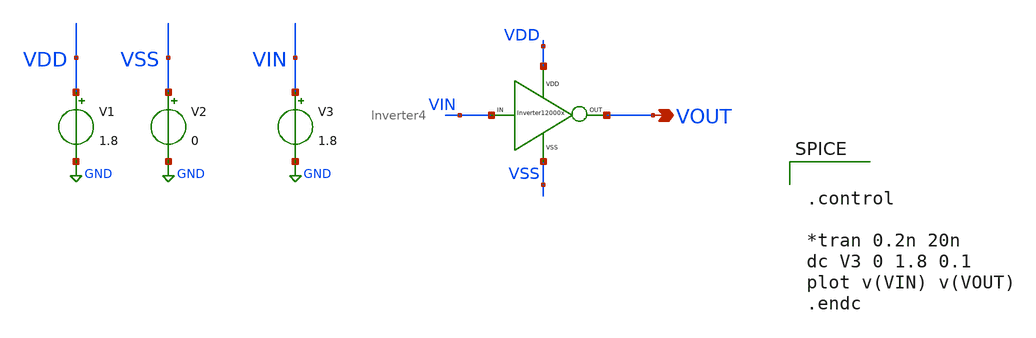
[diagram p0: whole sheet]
** sch_path: xschem/DC_DC_Converter_xschem/OTHERS/DC_DC_Converter0/Inverter_4/Inverter4_TB.sch
**.subckt Inverter4_TB VOUT
*.opin VOUT
V1 VDD GND 1.8
V2 VSS GND 0
V3 VIN GND 1.8
X1 VIN VOUT VDD VSS Inverter4
**** begin user architecture code


.control

*tran 0.2n 20n
dc V3 0 1.8 0.1
plot v(VIN) v(VOUT)
.endc



** opencircuitdesign pdks install
.lib $::SKYWATER_MODELS/sky130.lib.spice tt


**** end user architecture code
**.ends

* expanding   symbol:  DC_DC_Converter/Inverter_4/Inverter4.sym # of pins=4
** sym_path: xschem/DC_DC_Converter_xschem/OTHERS/DC_DC_Converter0/Inverter_4/Inverter4.sym
** sch_path: xschem/DC_DC_Converter_xschem/OTHERS/DC_DC_Converter0/Inverter_4/Inverter4.sch
.subckt Inverter4 VIN VOUT VDD VSS
*.ipin VIN
*.iopin VDD
*.iopin VSS
*.opin VOUT
XM1 net2 VIN VSS VSS sky130_fd_pr__nfet_01v8 L=0.15 W=40 nf=1 ad='int((nf+1)/2) * W/nf * 0.29' as='int((nf+2)/2) * W/nf * 0.29'
+ pd='2*int((nf+1)/2) * (W/nf + 0.29)' ps='2*int((nf+2)/2) * (W/nf + 0.29)' nrd='0.29 / W' nrs='0.29 / W'
+ sa=0 sb=0 sd=0 mult=300 m=300
XM2 net1 VIN VDD VDD sky130_fd_pr__pfet_01v8 L=0.15 W=12 nf=1 ad='int((nf+1)/2) * W/nf * 0.29' as='int((nf+2)/2) * W/nf * 0.29'
+ pd='2*int((nf+1)/2) * (W/nf + 0.29)' ps='2*int((nf+2)/2) * (W/nf + 0.29)' nrd='0.29 / W' nrs='0.29 / W'
+ sa=0 sb=0 sd=0 mult=3000 m=3000
RD net2 net1 sky130_fd_pr__res_generic_m1 W=1.25 L=10000 m=1
XM3 VOUT net1 VDD VDD sky130_fd_pr__pfet_01v8 L=0.15 W=3 nf=1 ad='int((nf+1)/2) * W/nf * 0.29' as='int((nf+2)/2) * W/nf * 0.29'
+ pd='2*int((nf+1)/2) * (W/nf + 0.29)' ps='2*int((nf+2)/2) * (W/nf + 0.29)' nrd='0.29 / W' nrs='0.29 / W'
+ sa=0 sb=0 sd=0 mult=1 m=1
XM4 VOUT net2 VSS VSS sky130_fd_pr__nfet_01v8 L=0.15 W=1 nf=1 ad='int((nf+1)/2) * W/nf * 0.29' as='int((nf+2)/2) * W/nf * 0.29'
+ pd='2*int((nf+1)/2) * (W/nf + 0.29)' ps='2*int((nf+2)/2) * (W/nf + 0.29)' nrd='0.29 / W' nrs='0.29 / W'
+ sa=0 sb=0 sd=0 mult=1 m=1
.ends

.GLOBAL GND
.end
